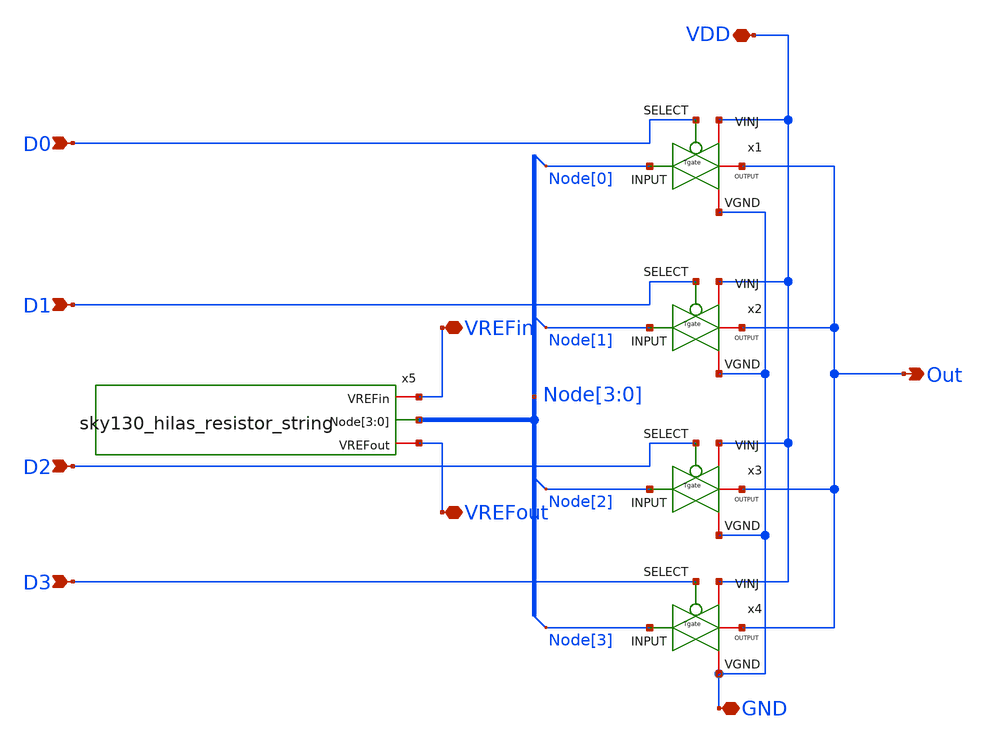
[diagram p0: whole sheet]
** sch_path: sky130_cells/RDAC/Design/sky130_hilas_dac_cell.sch
**.subckt sky130_hilas_dac_cell VDD Out D0 D1 D2 D3 GND VREFout VREFin
*.iopin VDD
*.opin Out
*.ipin D0
*.ipin D1
*.ipin D2
*.ipin D3
*.iopin GND
*.iopin VREFout
*.iopin VREFin
x1 VDD Out D0 Node[0] GND Tgate
x2 VDD Out D1 Node[1] GND Tgate
x3 VDD Out D2 Node[2] GND Tgate
x4 VDD Out D3 Node[3] GND Tgate
x5 VREFin Node[3] Node[2] Node[1] Node[0] VREFout sky130_hilas_resistor_string
**.ends

* expanding   symbol:  sky130_cells/RDAC/Design/Tgate.sym # of pins=5
** sym_path: sky130_cells/RDAC/Design/Tgate.sym
** sch_path: sky130_cells/RDAC/Design/Tgate.sch
.subckt Tgate VINJ OUTPUT SELECT INPUT VGND
*.iopin VINJ
*.ipin SELECT
*.iopin INPUT
*.iopin OUTPUT
*.ipin VGND
XM5 net1 SELECT VGND VGND sky130_fd_pr__nfet_g5v0d10v5 L=0.5 W=0.42 nf=1 ad='int((1 + 1)/2) * 0.42 / 1 * 0.29'
+ as='int((1 + 2)/2) * 0.42 / 1 * 0.29' pd='2*int((1 + 1)/2) * (0.42 / 1 + 0.29)' ps='2*int((1 + 2)/2) * (0.42 / 1 + 0.29)'
+ nrd='0.29 / 0.42 ' nrs='0.29 / 0.42 ' sa=0 sb=0 sd=0 mult=1 m=1
XM1 net1 SELECT VINJ VINJ sky130_fd_pr__pfet_g5v0d10v5 L=0.5 W=0.42 nf=1 ad='int((1 + 1)/2) * 0.42 / 1 * 0.29'
+ as='int((1 + 2)/2) * 0.42 / 1 * 0.29' pd='2*int((1 + 1)/2) * (0.42 / 1 + 0.29)' ps='2*int((1 + 2)/2) * (0.42 / 1 + 0.29)'
+ nrd='0.29 / 0.42 ' nrs='0.29 / 0.42 ' sa=0 sb=0 sd=0 mult=1 m=1
XM2 INPUT net1 OUTPUT VINJ sky130_fd_pr__pfet_g5v0d10v5 L=0.5 W=0.42 nf=1 ad='int((1 + 1)/2) * 0.42 / 1 * 0.29'
+ as='int((1 + 2)/2) * 0.42 / 1 * 0.29' pd='2*int((1 + 1)/2) * (0.42 / 1 + 0.29)' ps='2*int((1 + 2)/2) * (0.42 / 1 + 0.29)'
+ nrd='0.29 / 0.42 ' nrs='0.29 / 0.42 ' sa=0 sb=0 sd=0 mult=1 m=1
XM3 OUTPUT SELECT INPUT VGND sky130_fd_pr__nfet_g5v0d10v5 L=0.5 W=0.42 nf=1 ad='int((1 + 1)/2) * 0.42 / 1 * 0.29'
+ as='int((1 + 2)/2) * 0.42 / 1 * 0.29' pd='2*int((1 + 1)/2) * (0.42 / 1 + 0.29)' ps='2*int((1 + 2)/2) * (0.42 / 1 + 0.29)'
+ nrd='0.29 / 0.42 ' nrs='0.29 / 0.42 ' sa=0 sb=0 sd=0 mult=1 m=1
.ends


* expanding   symbol:  sky130_cells/RDAC/Design/sky130_hilas_resistor_string.sym # of pins=3
** sym_path: sky130_cells/RDAC/Design/sky130_hilas_resistor_string.sym
** sch_path: sky130_cells/RDAC/Design/sky130_hilas_resistor_string.sch
.subckt sky130_hilas_resistor_string VREFin Node[3] Node[2] Node[1] Node[0] VREFout
*.iopin VREFout
*.iopin VREFin
*.opin Node[3],Node[2],Node[1],Node[0]
XR1 Node[0] VREFin sky130_fd_pr__res_generic_po W=0.33 L=10.19 m=1
XR2 net1 Node[0] sky130_fd_pr__res_generic_po W=0.33 L=10.19 m=1
XR3 Node[1] net1 sky130_fd_pr__res_generic_po W=0.33 L=10.19 m=1
XR4 net2 Node[1] sky130_fd_pr__res_generic_po W=0.33 L=10.19 m=1
XR5 Node[2] net2 sky130_fd_pr__res_generic_po W=0.33 L=10.19 m=1
XR6 net3 Node[2] sky130_fd_pr__res_generic_po W=0.33 L=10.19 m=1
XR7 Node[3] net3 sky130_fd_pr__res_generic_po W=0.33 L=10.19 m=1
XR8 VREFout Node[3] sky130_fd_pr__res_generic_po W=0.33 L=10.19 m=1
.ends

.end
